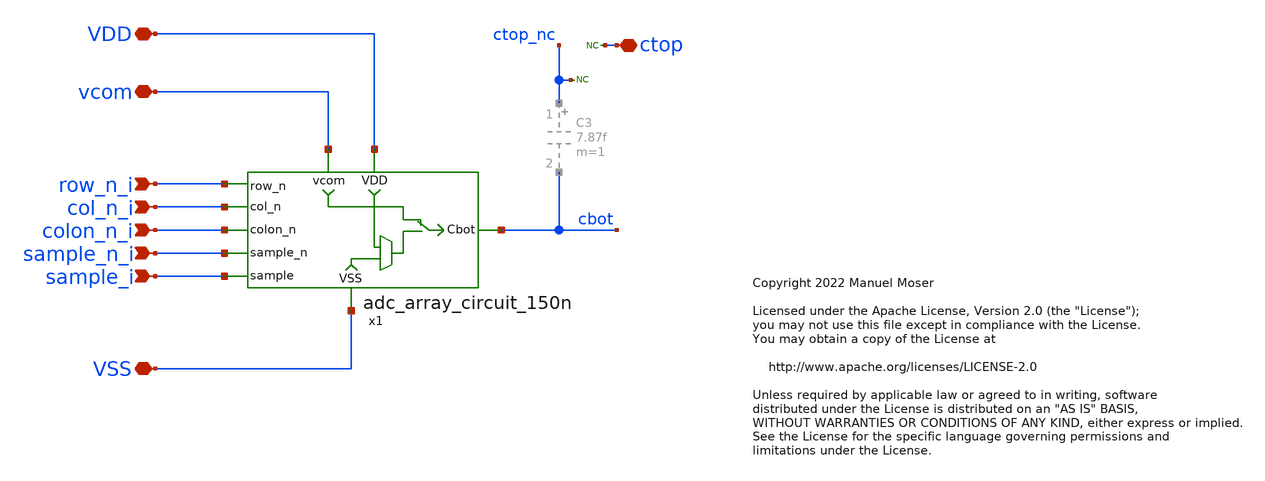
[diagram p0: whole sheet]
** sch_path: xschem/adc_array_cap/adc_array_cap_dummy.sch
* Copyright 2022 Manuel Moser
* Licensed under the Apache License, Version 2.0 (the "License");
**.subckt adc_array_cap_dummy vcom VDD ctop VSS row_n_i col_n_i colon_n_i sample_n_i sample_i
*.iopin vcom
*.iopin VDD
*.iopin ctop
*.iopin VSS
*.ipin row_n_i
*.ipin col_n_i
*.ipin colon_n_i
*.ipin sample_n_i
*.ipin sample_i
x1 VDD row_n_i cbot col_n_i colon_n_i sample_n_i vcom sample_i VSS adc_array_circuit_150n
* noconn ctop
* noconn ctop_nc
**.ends

* expanding   symbol:
*+  /foss/designs/SKY130_SAR-ADC/xschem/adc_array_circuit/adc_array_circuit_150n.sym # of pins=9
** sym_path: xschem/adc_array_circuit_150n/adc_array_circuit_150n.sym
** sch_path: xschem/adc_array_circuit_150n/adc_array_circuit_150n.sch
.subckt adc_array_circuit_150n VDD row_n Cbot col_n colon_n sample_n vcom sample VSS
*.ipin sample_n
*.ipin sample
*.iopin vcom
*.ipin row_n
*.ipin col_n
*.ipin colon_n
*.iopin VDD
*.iopin VSS
*.iopin Cbot
XM1 vcom sample Cbot VSS sky130_fd_pr__nfet_01v8 L=0.15 W=0.42 nf=1 ad='int((nf+1)/2) * W/nf * 0.29'
+ as='int((nf+2)/2) * W/nf * 0.29' pd='2*int((nf+1)/2) * (W/nf + 0.29)' ps='2*int((nf+2)/2) * (W/nf + 0.29)'
+ nrd='0.29 / W' nrs='0.29 / W' sa=0 sb=0 sd=0 mult=1 m=1
XM3 vcom sample_n Cbot VDD sky130_fd_pr__pfet_01v8 L=0.15 W=0.8 nf=1 ad='int((nf+1)/2) * W/nf * 0.29'
+ as='int((nf+2)/2) * W/nf * 0.29' pd='2*int((nf+1)/2) * (W/nf + 0.29)' ps='2*int((nf+2)/2) * (W/nf + 0.29)'
+ nrd='0.29 / W' nrs='0.29 / W' sa=0 sb=0 sd=0 mult=1 m=1
XM2 vdrv sample_n Cbot VSS sky130_fd_pr__nfet_01v8 L=0.15 W=0.42 nf=1 ad='int((nf+1)/2) * W/nf * 0.29'
+ as='int((nf+2)/2) * W/nf * 0.29' pd='2*int((nf+1)/2) * (W/nf + 0.29)' ps='2*int((nf+2)/2) * (W/nf + 0.29)'
+ nrd='0.29 / W' nrs='0.29 / W' sa=0 sb=0 sd=0 mult=1 m=1
XM4 vdrv sample Cbot VDD sky130_fd_pr__pfet_01v8 L=0.15 W=0.8 nf=1 ad='int((nf+1)/2) * W/nf * 0.29' as='int((nf+2)/2) * W/nf * 0.29'
+ pd='2*int((nf+1)/2) * (W/nf + 0.29)' ps='2*int((nf+2)/2) * (W/nf + 0.29)' nrd='0.29 / W' nrs='0.29 / W'
+ sa=0 sb=0 sd=0 mult=1 m=1
XM5 vint1 col_n vdrv VDD sky130_fd_pr__pfet_01v8 L=0.15 W=0.8 nf=1 ad='int((nf+1)/2) * W/nf * 0.29' as='int((nf+2)/2) * W/nf * 0.29'
+ pd='2*int((nf+1)/2) * (W/nf + 0.29)' ps='2*int((nf+2)/2) * (W/nf + 0.29)' nrd='0.29 / W' nrs='0.29 / W'
+ sa=0 sb=0 sd=0 mult=1 m=1
XM6 VDD row_n vint1 VDD sky130_fd_pr__pfet_01v8 L=0.15 W=0.8 nf=1 ad='int((nf+1)/2) * W/nf * 0.29' as='int((nf+2)/2) * W/nf * 0.29'
+ pd='2*int((nf+1)/2) * (W/nf + 0.29)' ps='2*int((nf+2)/2) * (W/nf + 0.29)' nrd='0.29 / W' nrs='0.29 / W'
+ sa=0 sb=0 sd=0 mult=1 m=1
XM7 VDD colon_n vdrv VDD sky130_fd_pr__pfet_01v8 L=0.15 W=0.8 nf=1 ad='int((nf+1)/2) * W/nf * 0.29' as='int((nf+2)/2) * W/nf * 0.29'
+ pd='2*int((nf+1)/2) * (W/nf + 0.29)' ps='2*int((nf+2)/2) * (W/nf + 0.29)' nrd='0.29 / W' nrs='0.29 / W'
+ sa=0 sb=0 sd=0 mult=1 m=1
XM8 vint2 colon_n vdrv VSS sky130_fd_pr__nfet_01v8 L=0.15 W=0.42 nf=1 ad='int((nf+1)/2) * W/nf * 0.29'
+ as='int((nf+2)/2) * W/nf * 0.29' pd='2*int((nf+1)/2) * (W/nf + 0.29)' ps='2*int((nf+2)/2) * (W/nf + 0.29)'
+ nrd='0.29 / W' nrs='0.29 / W' sa=0 sb=0 sd=0 mult=1 m=1
XM9 VSS row_n vint2 VSS sky130_fd_pr__nfet_01v8 L=0.15 W=0.42 nf=1 ad='int((nf+1)/2) * W/nf * 0.29' as='int((nf+2)/2) * W/nf * 0.29'
+ pd='2*int((nf+1)/2) * (W/nf + 0.29)' ps='2*int((nf+2)/2) * (W/nf + 0.29)' nrd='0.29 / W' nrs='0.29 / W'
+ sa=0 sb=0 sd=0 mult=1 m=1
XM10 VSS col_n vint2 VSS sky130_fd_pr__nfet_01v8 L=0.15 W=0.42 nf=1 ad='int((nf+1)/2) * W/nf * 0.29'
+ as='int((nf+2)/2) * W/nf * 0.29' pd='2*int((nf+1)/2) * (W/nf + 0.29)' ps='2*int((nf+2)/2) * (W/nf + 0.29)'
+ nrd='0.29 / W' nrs='0.29 / W' sa=0 sb=0 sd=0 mult=1 m=1
.ends

.end
